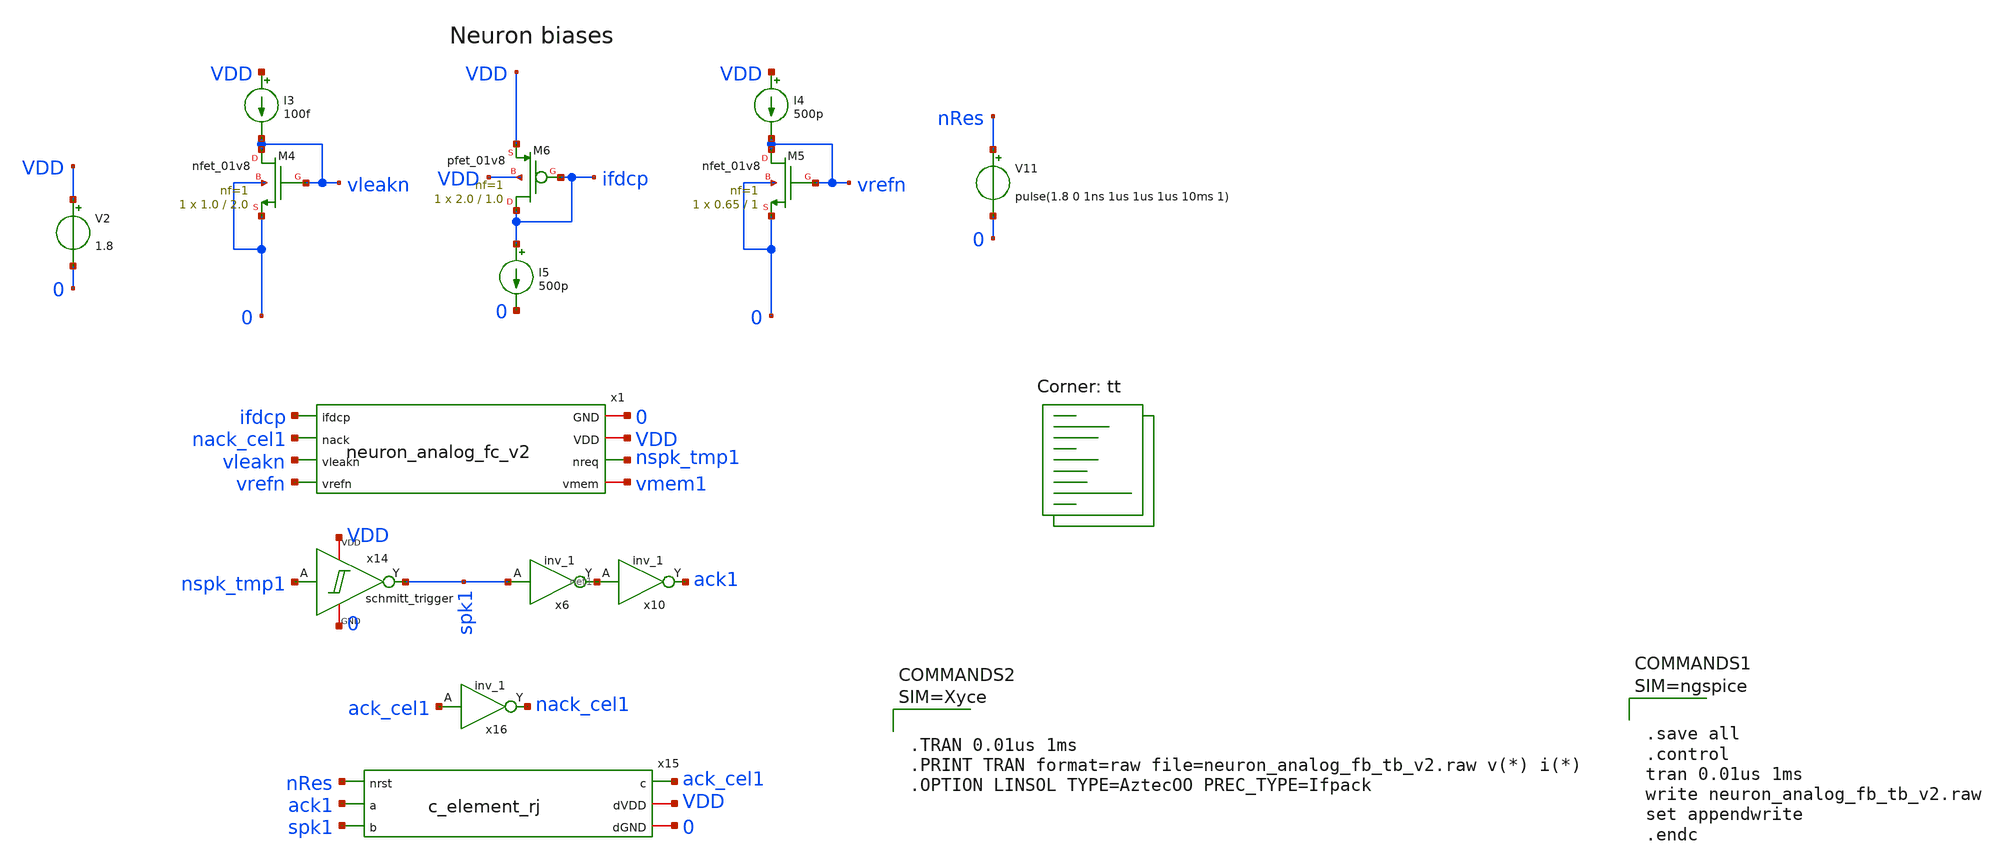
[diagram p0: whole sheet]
** sch_path: design/xschem/neuron_analog_fc_v2_tb.sch
**.subckt neuron_analog_fc_v2_tb
x1 0 VDD nspk_tmp1 ifdcp nack_cel1 vmem1 vleakn vrefn neuron_analog_fc_v2
V2 VDD 0 1.8
I3 VDD vleakn 100f
XM4 vleakn vleakn 0 0 sky130_fd_pr__nfet_01v8 L=2.0 W=1.0 nf=1 ad='int((nf+1)/2) * W/nf * 0.29' as='int((nf+2)/2) * W/nf * 0.29'
+ pd='2*int((nf+1)/2) * (W/nf + 0.29)' ps='2*int((nf+2)/2) * (W/nf + 0.29)' nrd='0.29 / W' nrs='0.29 / W'
+ sa=0 sb=0 sd=0 mult=1 m=1
XM6 ifdcp ifdcp VDD VDD sky130_fd_pr__pfet_01v8 L=1.0 W=2.0 nf=1 ad='int((nf+1)/2) * W/nf * 0.29' as='int((nf+2)/2) * W/nf * 0.29'
+ pd='2*int((nf+1)/2) * (W/nf + 0.29)' ps='2*int((nf+2)/2) * (W/nf + 0.29)' nrd='0.29 / W' nrs='0.29 / W'
+ sa=0 sb=0 sd=0 mult=1 m=1
I5 ifdcp 0 500p
I4 VDD vrefn 500p
XM5 vrefn vrefn 0 0 sky130_fd_pr__nfet_01v8 L=1 W=0.65 nf=1 ad='int((nf+1)/2) * W/nf * 0.29' as='int((nf+2)/2) * W/nf * 0.29'
+ pd='2*int((nf+1)/2) * (W/nf + 0.29)' ps='2*int((nf+2)/2) * (W/nf + 0.29)' nrd='0.29 / W' nrs='0.29 / W'
+ sa=0 sb=0 sd=0 mult=1 m=1
x16 ack_cel1 0 0 VDD VDD nack_cel1 sky130_fd_sc_hd__inv_1
x6 spk1 0 0 VDD VDD net1 sky130_fd_sc_hd__inv_1
x10 net1 0 0 VDD VDD ack1 sky130_fd_sc_hd__inv_1
x14 nspk_tmp1 spk1 VDD 0 schmitt_trigger
x15 nRes ack1 spk1 ack_cel1 VDD 0 c_element_rj
V11 nRes 0 pulse(1.8 0 1ns 1us 1us 1us 10ms 1)
**** begin user architecture code



.save all
.control
tran 0.01us 1ms
write neuron_analog_fb_tb_v2.raw
set appendwrite
.endc



.lib $::SKYWATER_MODELS/sky130.lib.spice tt


* Standard cell simulation files
.include $::SKYWATER_STDCELLS/sky130_fd_sc_hd.spice




**** end user architecture code
**.ends

* expanding   symbol:  neuron_analog_fc_v2.sym # of pins=8
** sym_path: design/xschem/neuron_analog_fc_v2.sym
** sch_path: design/xschem/neuron_analog_fc_v2.sch
.subckt neuron_analog_fc_v2 GND VDD nreq ifdcp nack vmem vleakn vrefn
*.ipin vleakn
*.iopin GND
*.iopin VDD
*.opin nreq
*.ipin vrefn
*.ipin nack
*.ipin ifdcp
*.iopin vmem
XC1 GND vmem sky130_fd_pr__cap_mim_m3_1 W=5 L=5 MF=1 m=1
XM1 vmem ifdcp VDD VDD sky130_fd_pr__pfet_01v8 L=2.0 W=1.0 nf=1 ad='int((nf+1)/2) * W/nf * 0.29' as='int((nf+2)/2) * W/nf * 0.29'
+ pd='2*int((nf+1)/2) * (W/nf + 0.29)' ps='2*int((nf+2)/2) * (W/nf + 0.29)' nrd='0.29 / W' nrs='0.29 / W'
+ sa=0 sb=0 sd=0 mult=1 m=1
XM5 net2 nreq VDD VDD sky130_fd_pr__pfet_01v8 L=0.25 W=1.0 nf=1 ad='int((nf+1)/2) * W/nf * 0.29' as='int((nf+2)/2) * W/nf * 0.29'
+ pd='2*int((nf+1)/2) * (W/nf + 0.29)' ps='2*int((nf+2)/2) * (W/nf + 0.29)' nrd='0.29 / W' nrs='0.29 / W'
+ sa=0 sb=0 sd=0 mult=1 m=1
XM7 net3 nreq net4 GND sky130_fd_pr__nfet_01v8 L=0.15 W=0.6 nf=1 ad='int((nf+1)/2) * W/nf * 0.29' as='int((nf+2)/2) * W/nf * 0.29'
+ pd='2*int((nf+1)/2) * (W/nf + 0.29)' ps='2*int((nf+2)/2) * (W/nf + 0.29)' nrd='0.29 / W' nrs='0.29 / W'
+ sa=0 sb=0 sd=0 mult=1 m=1
XM6 net5 nack VDD VDD sky130_fd_pr__pfet_01v8 L=0.25 W=1.0 nf=1 ad='int((nf+1)/2) * W/nf * 0.29' as='int((nf+2)/2) * W/nf * 0.29'
+ pd='2*int((nf+1)/2) * (W/nf + 0.29)' ps='2*int((nf+2)/2) * (W/nf + 0.29)' nrd='0.29 / W' nrs='0.29 / W'
+ sa=0 sb=0 sd=0 mult=1 m=1
XM9 nreq vmem net2 VDD sky130_fd_pr__pfet_01v8 L=0.15 W=1.0 nf=1 ad='int((nf+1)/2) * W/nf * 0.29' as='int((nf+2)/2) * W/nf * 0.29'
+ pd='2*int((nf+1)/2) * (W/nf + 0.29)' ps='2*int((nf+2)/2) * (W/nf + 0.29)' nrd='0.29 / W' nrs='0.29 / W'
+ sa=0 sb=0 sd=0 mult=1 m=1
XM10 net3 nreq net5 VDD sky130_fd_pr__pfet_01v8 L=0.15 W=1.0 nf=1 ad='int((nf+1)/2) * W/nf * 0.29' as='int((nf+2)/2) * W/nf * 0.29'
+ pd='2*int((nf+1)/2) * (W/nf + 0.29)' ps='2*int((nf+2)/2) * (W/nf + 0.29)' nrd='0.29 / W' nrs='0.29 / W'
+ sa=0 sb=0 sd=0 mult=1 m=1
XM4 vmem nreq VDD VDD sky130_fd_pr__pfet_01v8 L=1.0 W=1.0 nf=1 ad='int((nf+1)/2) * W/nf * 0.29' as='int((nf+2)/2) * W/nf * 0.29'
+ pd='2*int((nf+1)/2) * (W/nf + 0.29)' ps='2*int((nf+2)/2) * (W/nf + 0.29)' nrd='0.29 / W' nrs='0.29 / W'
+ sa=0 sb=0 sd=0 mult=1 m=1
XM2 nreq vmem net1 GND sky130_fd_pr__nfet_01v8 L=0.15 W=0.6 nf=1 ad='int((nf+1)/2) * W/nf * 0.29' as='int((nf+2)/2) * W/nf * 0.29'
+ pd='2*int((nf+1)/2) * (W/nf + 0.29)' ps='2*int((nf+2)/2) * (W/nf + 0.29)' nrd='0.29 / W' nrs='0.29 / W'
+ sa=0 sb=0 sd=0 mult=1 m=1
XM3 net4 vrefn GND GND sky130_fd_pr__nfet_01v8 L=1.0 W=0.6 nf=1 ad='int((nf+1)/2) * W/nf * 0.29' as='int((nf+2)/2) * W/nf * 0.29'
+ pd='2*int((nf+1)/2) * (W/nf + 0.29)' ps='2*int((nf+2)/2) * (W/nf + 0.29)' nrd='0.29 / W' nrs='0.29 / W'
+ sa=0 sb=0 sd=0 mult=1 m=1
XM8 net1 net1 GND GND sky130_fd_pr__nfet_01v8 L=0.15 W=0.6 nf=1 ad='int((nf+1)/2) * W/nf * 0.29' as='int((nf+2)/2) * W/nf * 0.29'
+ pd='2*int((nf+1)/2) * (W/nf + 0.29)' ps='2*int((nf+2)/2) * (W/nf + 0.29)' nrd='0.29 / W' nrs='0.29 / W'
+ sa=0 sb=0 sd=0 mult=1 m=1
XM11 vmem net3 GND GND sky130_fd_pr__nfet_01v8 L=0.2 W=1.0 nf=1 ad='int((nf+1)/2) * W/nf * 0.29' as='int((nf+2)/2) * W/nf * 0.29'
+ pd='2*int((nf+1)/2) * (W/nf + 0.29)' ps='2*int((nf+2)/2) * (W/nf + 0.29)' nrd='0.29 / W' nrs='0.29 / W'
+ sa=0 sb=0 sd=0 mult=1 m=1
XM12 vmem vleakn GND GND sky130_fd_pr__nfet_01v8 L=2.0 W=1.0 nf=1 ad='int((nf+1)/2) * W/nf * 0.29' as='int((nf+2)/2) * W/nf * 0.29'
+ pd='2*int((nf+1)/2) * (W/nf + 0.29)' ps='2*int((nf+2)/2) * (W/nf + 0.29)' nrd='0.29 / W' nrs='0.29 / W'
+ sa=0 sb=0 sd=0 mult=1 m=1
XM13 GND net3 GND GND sky130_fd_pr__nfet_01v8 L=2.0 W=1.0 nf=1 ad='int((nf+1)/2) * W/nf * 0.29' as='int((nf+2)/2) * W/nf * 0.29'
+ pd='2*int((nf+1)/2) * (W/nf + 0.29)' ps='2*int((nf+2)/2) * (W/nf + 0.29)' nrd='0.29 / W' nrs='0.29 / W'
+ sa=0 sb=0 sd=0 mult=1 m=1
.ends


* expanding   symbol:  schmitt_trigger.sym # of pins=4
** sym_path: design/xschem/schmitt_trigger.sym
** sch_path: design/xschem/schmitt_trigger.sch
.subckt schmitt_trigger A Y VDD GND
*.ipin A
*.opin Y
*.iopin VDD
*.iopin GND
XM3 net2 A GND GND sky130_fd_pr__nfet_01v8 L=0.15 W=0.65 nf=1 ad='int((nf+1)/2) * W/nf * 0.29' as='int((nf+2)/2) * W/nf * 0.29'
+ pd='2*int((nf+1)/2) * (W/nf + 0.29)' ps='2*int((nf+2)/2) * (W/nf + 0.29)' nrd='0.29 / W' nrs='0.29 / W'
+ sa=0 sb=0 sd=0 mult=1 m=1
XM1 Y A net2 GND sky130_fd_pr__nfet_01v8 L=0.15 W=0.65 nf=1 ad='int((nf+1)/2) * W/nf * 0.29' as='int((nf+2)/2) * W/nf * 0.29'
+ pd='2*int((nf+1)/2) * (W/nf + 0.29)' ps='2*int((nf+2)/2) * (W/nf + 0.29)' nrd='0.29 / W' nrs='0.29 / W'
+ sa=0 sb=0 sd=0 mult=1 m=1
XM7 VDD Y net2 GND sky130_fd_pr__nfet_01v8 L=0.15 W=0.42 nf=1 ad='int((nf+1)/2) * W/nf * 0.29' as='int((nf+2)/2) * W/nf * 0.29'
+ pd='2*int((nf+1)/2) * (W/nf + 0.29)' ps='2*int((nf+2)/2) * (W/nf + 0.29)' nrd='0.29 / W' nrs='0.29 / W'
+ sa=0 sb=0 sd=0 mult=1 m=1
XM4 net1 A VDD VDD sky130_fd_pr__pfet_01v8 L=0.15 W=1 nf=1 ad='int((nf+1)/2) * W/nf * 0.29' as='int((nf+2)/2) * W/nf * 0.29'
+ pd='2*int((nf+1)/2) * (W/nf + 0.29)' ps='2*int((nf+2)/2) * (W/nf + 0.29)' nrd='0.29 / W' nrs='0.29 / W'
+ sa=0 sb=0 sd=0 mult=1 m=1
XM2 Y A net1 VDD sky130_fd_pr__pfet_01v8 L=0.15 W=1 nf=1 ad='int((nf+1)/2) * W/nf * 0.29' as='int((nf+2)/2) * W/nf * 0.29'
+ pd='2*int((nf+1)/2) * (W/nf + 0.29)' ps='2*int((nf+2)/2) * (W/nf + 0.29)' nrd='0.29 / W' nrs='0.29 / W'
+ sa=0 sb=0 sd=0 mult=1 m=1
XM5 GND Y net1 VDD sky130_fd_pr__pfet_01v8 L=0.15 W=0.82 nf=1 ad='int((nf+1)/2) * W/nf * 0.29' as='int((nf+2)/2) * W/nf * 0.29'
+ pd='2*int((nf+1)/2) * (W/nf + 0.29)' ps='2*int((nf+2)/2) * (W/nf + 0.29)' nrd='0.29 / W' nrs='0.29 / W'
+ sa=0 sb=0 sd=0 mult=1 m=1
.ends


* expanding   symbol:  c_element_rj.sym # of pins=6
** sym_path: design/xschem/c_element_rj.sym
** sch_path: design/xschem/c_element_rj.sch
.subckt c_element_rj nrst a b c dVDD dGND
*.iopin dGND
*.iopin dVDD
*.opin c
*.ipin b
*.ipin a
*.ipin nrst
XM14 c net6 dVDD dVDD sky130_fd_pr__pfet_01v8 L=0.15 W=1 nf=1 ad='int((nf+1)/2) * W/nf * 0.29' as='int((nf+2)/2) * W/nf * 0.29'
+ pd='2*int((nf+1)/2) * (W/nf + 0.29)' ps='2*int((nf+2)/2) * (W/nf + 0.29)' nrd='0.29 / W' nrs='0.29 / W'
+ sa=0 sb=0 sd=0 mult=1 m=1
XM5 net6 nrst dVDD dVDD sky130_fd_pr__pfet_01v8 L=0.15 W=1 nf=1 ad='int((nf+1)/2) * W/nf * 0.29' as='int((nf+2)/2) * W/nf * 0.29'
+ pd='2*int((nf+1)/2) * (W/nf + 0.29)' ps='2*int((nf+2)/2) * (W/nf + 0.29)' nrd='0.29 / W' nrs='0.29 / W'
+ sa=0 sb=0 sd=0 mult=1 m=1
XM6 net5 b dVDD dVDD sky130_fd_pr__pfet_01v8 L=0.15 W=1 nf=1 ad='int((nf+1)/2) * W/nf * 0.29' as='int((nf+2)/2) * W/nf * 0.29'
+ pd='2*int((nf+1)/2) * (W/nf + 0.29)' ps='2*int((nf+2)/2) * (W/nf + 0.29)' nrd='0.29 / W' nrs='0.29 / W'
+ sa=0 sb=0 sd=0 mult=1 m=1
XM4 net4 a dVDD dVDD sky130_fd_pr__pfet_01v8 L=0.15 W=1 nf=1 ad='int((nf+1)/2) * W/nf * 0.29' as='int((nf+2)/2) * W/nf * 0.29'
+ pd='2*int((nf+1)/2) * (W/nf + 0.29)' ps='2*int((nf+2)/2) * (W/nf + 0.29)' nrd='0.29 / W' nrs='0.29 / W'
+ sa=0 sb=0 sd=0 mult=1 m=1
XM7 net3 b net4 dVDD sky130_fd_pr__pfet_01v8 L=0.15 W=1 nf=1 ad='int((nf+1)/2) * W/nf * 0.29' as='int((nf+2)/2) * W/nf * 0.29'
+ pd='2*int((nf+1)/2) * (W/nf + 0.29)' ps='2*int((nf+2)/2) * (W/nf + 0.29)' nrd='0.29 / W' nrs='0.29 / W'
+ sa=0 sb=0 sd=0 mult=1 m=1
XM8 net3 a net5 dVDD sky130_fd_pr__pfet_01v8 L=0.15 W=1 nf=1 ad='int((nf+1)/2) * W/nf * 0.29' as='int((nf+2)/2) * W/nf * 0.29'
+ pd='2*int((nf+1)/2) * (W/nf + 0.29)' ps='2*int((nf+2)/2) * (W/nf + 0.29)' nrd='0.29 / W' nrs='0.29 / W'
+ sa=0 sb=0 sd=0 mult=1 m=1
XM10 net5 c net4 dVDD sky130_fd_pr__pfet_01v8 L=0.15 W=1 nf=1 ad='int((nf+1)/2) * W/nf * 0.29' as='int((nf+2)/2) * W/nf * 0.29'
+ pd='2*int((nf+1)/2) * (W/nf + 0.29)' ps='2*int((nf+2)/2) * (W/nf + 0.29)' nrd='0.29 / W' nrs='0.29 / W'
+ sa=0 sb=0 sd=0 mult=1 m=1
XM12 c net6 dGND dGND sky130_fd_pr__nfet_01v8 L=0.15 W=0.65 nf=1 ad='int((nf+1)/2) * W/nf * 0.29' as='int((nf+2)/2) * W/nf * 0.29'
+ pd='2*int((nf+1)/2) * (W/nf + 0.29)' ps='2*int((nf+2)/2) * (W/nf + 0.29)' nrd='0.29 / W' nrs='0.29 / W'
+ sa=0 sb=0 sd=0 mult=1 m=1
XM1 net3 nrst net6 dGND sky130_fd_pr__nfet_01v8 L=0.15 W=0.65 nf=1 ad='int((nf+1)/2) * W/nf * 0.29' as='int((nf+2)/2) * W/nf * 0.29'
+ pd='2*int((nf+1)/2) * (W/nf + 0.29)' ps='2*int((nf+2)/2) * (W/nf + 0.29)' nrd='0.29 / W' nrs='0.29 / W'
+ sa=0 sb=0 sd=0 mult=1 m=1
XM2 net3 b net1 dGND sky130_fd_pr__nfet_01v8 L=0.15 W=0.65 nf=1 ad='int((nf+1)/2) * W/nf * 0.29' as='int((nf+2)/2) * W/nf * 0.29'
+ pd='2*int((nf+1)/2) * (W/nf + 0.29)' ps='2*int((nf+2)/2) * (W/nf + 0.29)' nrd='0.29 / W' nrs='0.29 / W'
+ sa=0 sb=0 sd=0 mult=1 m=1
XM3 net3 a net2 dGND sky130_fd_pr__nfet_01v8 L=0.15 W=0.65 nf=1 ad='int((nf+1)/2) * W/nf * 0.29' as='int((nf+2)/2) * W/nf * 0.29'
+ pd='2*int((nf+1)/2) * (W/nf + 0.29)' ps='2*int((nf+2)/2) * (W/nf + 0.29)' nrd='0.29 / W' nrs='0.29 / W'
+ sa=0 sb=0 sd=0 mult=1 m=1
XM9 net2 c net1 dGND sky130_fd_pr__nfet_01v8 L=0.15 W=0.65 nf=1 ad='int((nf+1)/2) * W/nf * 0.29' as='int((nf+2)/2) * W/nf * 0.29'
+ pd='2*int((nf+1)/2) * (W/nf + 0.29)' ps='2*int((nf+2)/2) * (W/nf + 0.29)' nrd='0.29 / W' nrs='0.29 / W'
+ sa=0 sb=0 sd=0 mult=1 m=1
XM11 net1 a dGND dGND sky130_fd_pr__nfet_01v8 L=0.15 W=0.65 nf=1 ad='int((nf+1)/2) * W/nf * 0.29' as='int((nf+2)/2) * W/nf * 0.29'
+ pd='2*int((nf+1)/2) * (W/nf + 0.29)' ps='2*int((nf+2)/2) * (W/nf + 0.29)' nrd='0.29 / W' nrs='0.29 / W'
+ sa=0 sb=0 sd=0 mult=1 m=1
XM13 net2 b dGND dGND sky130_fd_pr__nfet_01v8 L=0.15 W=0.65 nf=1 ad='int((nf+1)/2) * W/nf * 0.29' as='int((nf+2)/2) * W/nf * 0.29'
+ pd='2*int((nf+1)/2) * (W/nf + 0.29)' ps='2*int((nf+2)/2) * (W/nf + 0.29)' nrd='0.29 / W' nrs='0.29 / W'
+ sa=0 sb=0 sd=0 mult=1 m=1
.ends

.end
